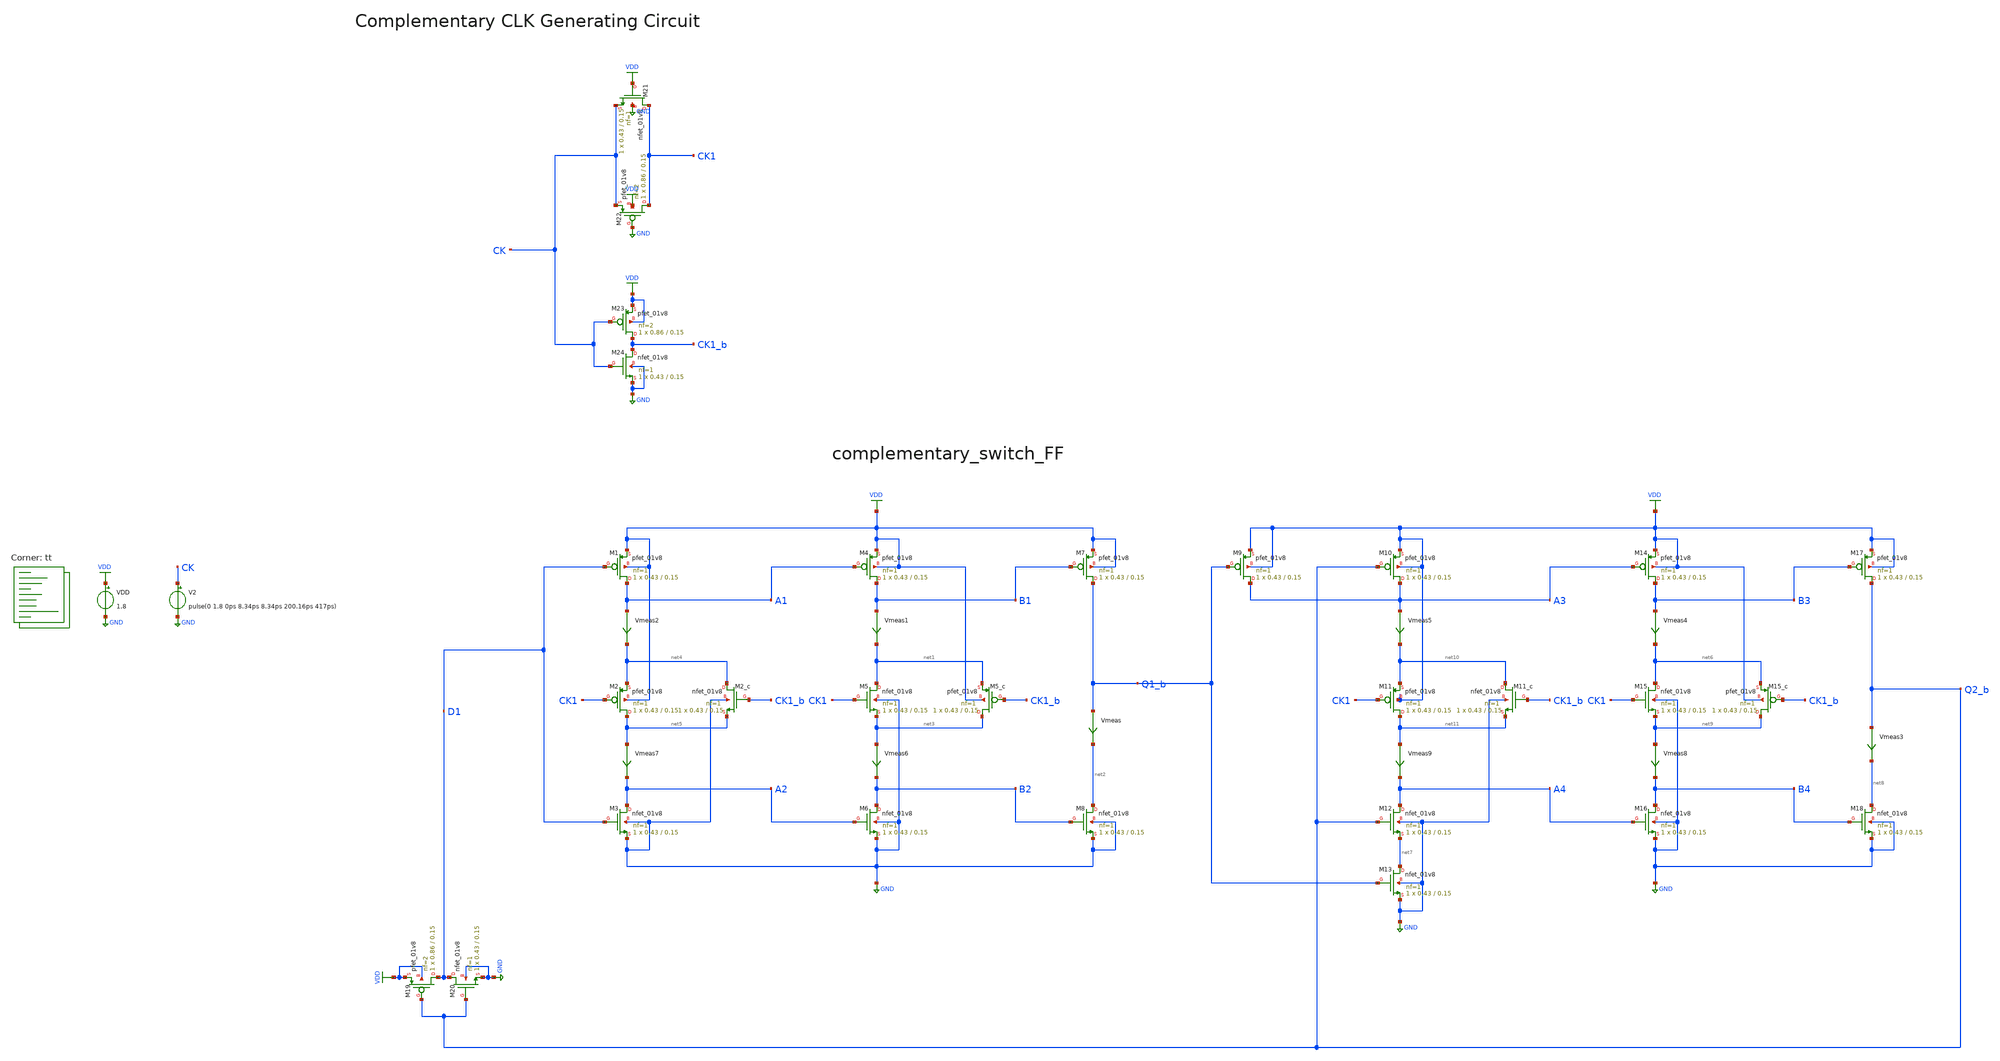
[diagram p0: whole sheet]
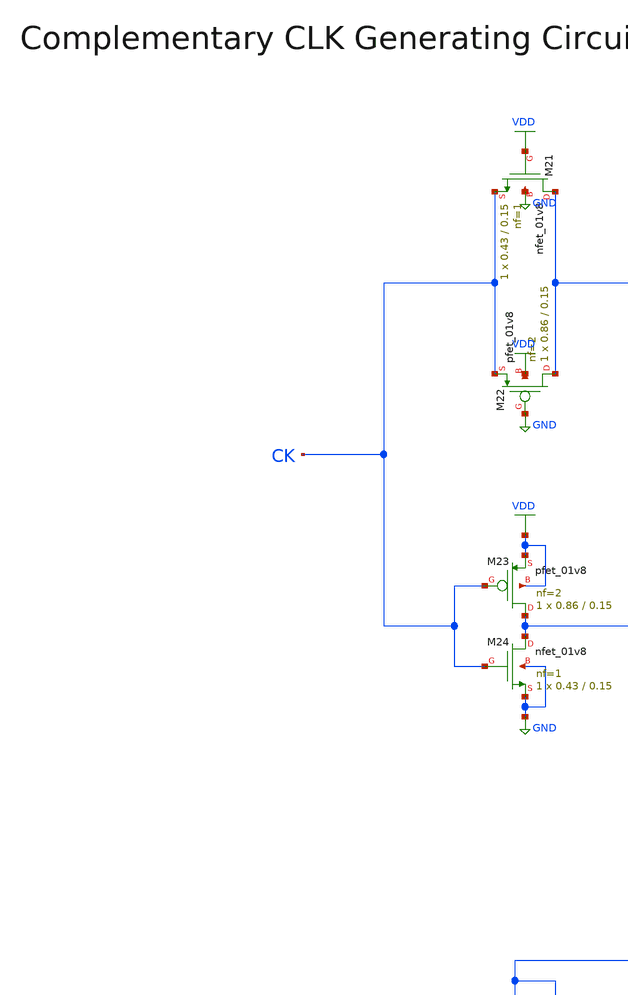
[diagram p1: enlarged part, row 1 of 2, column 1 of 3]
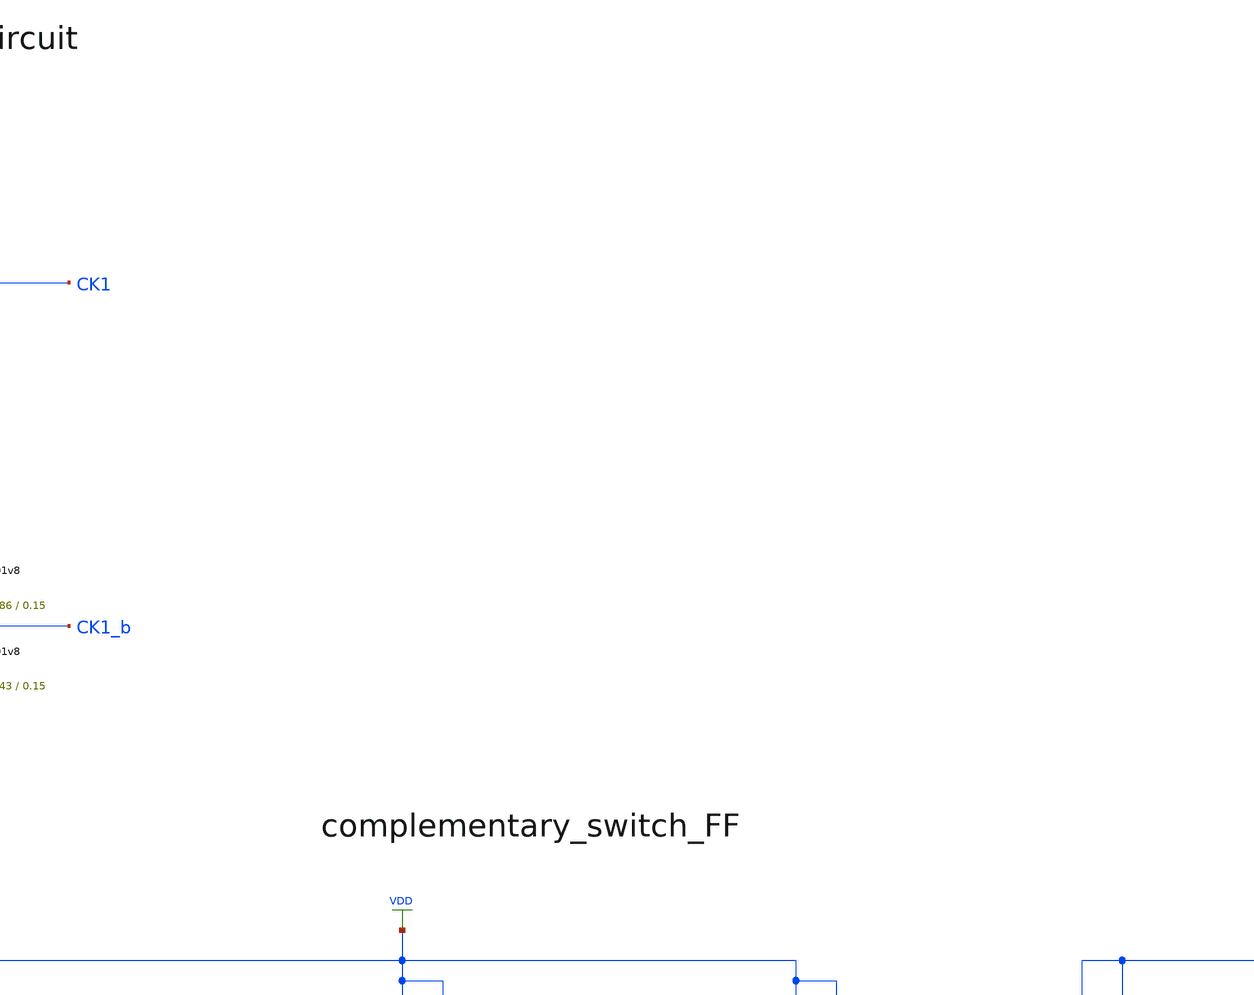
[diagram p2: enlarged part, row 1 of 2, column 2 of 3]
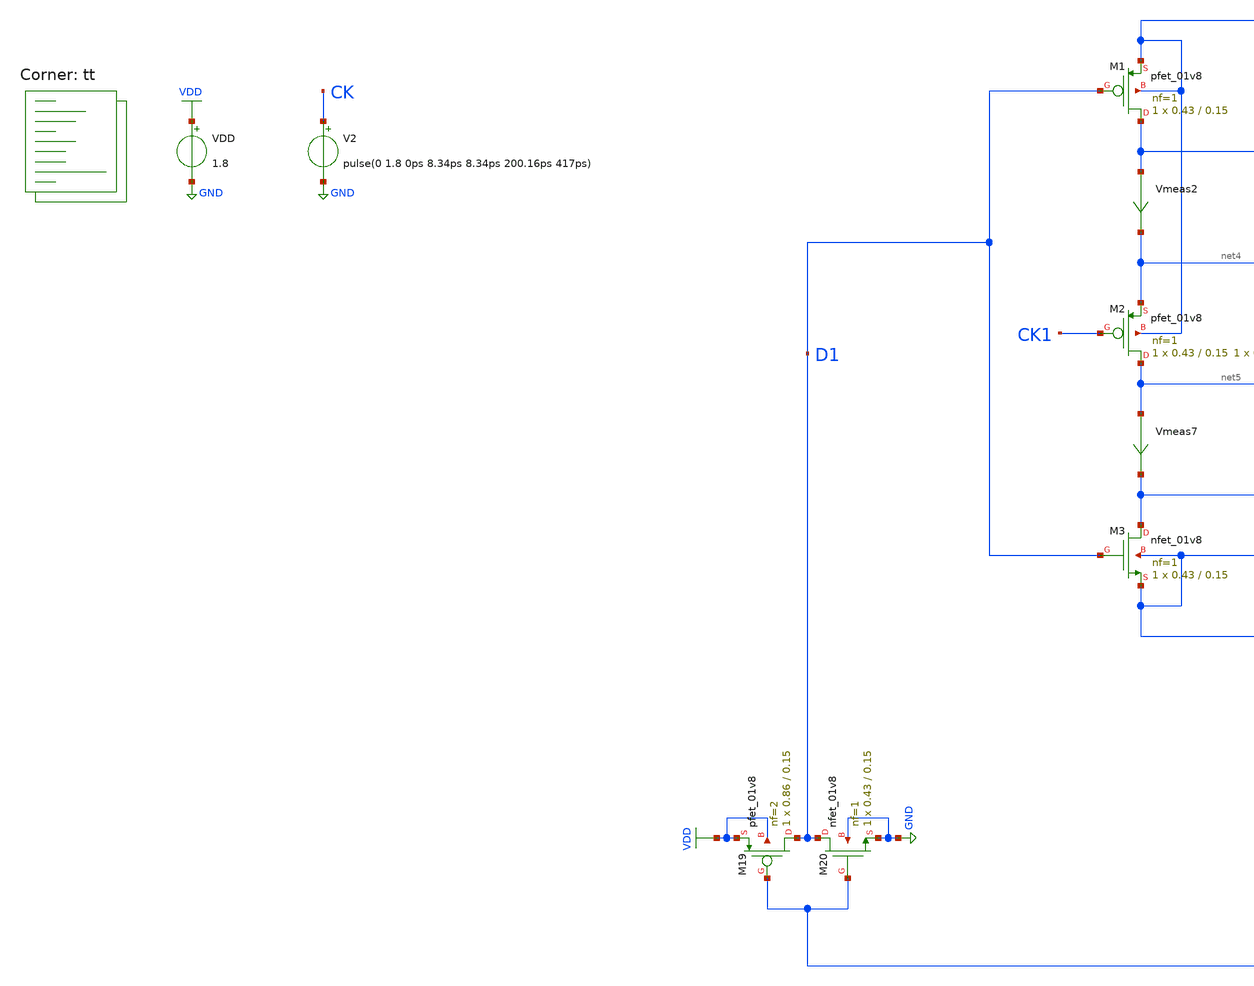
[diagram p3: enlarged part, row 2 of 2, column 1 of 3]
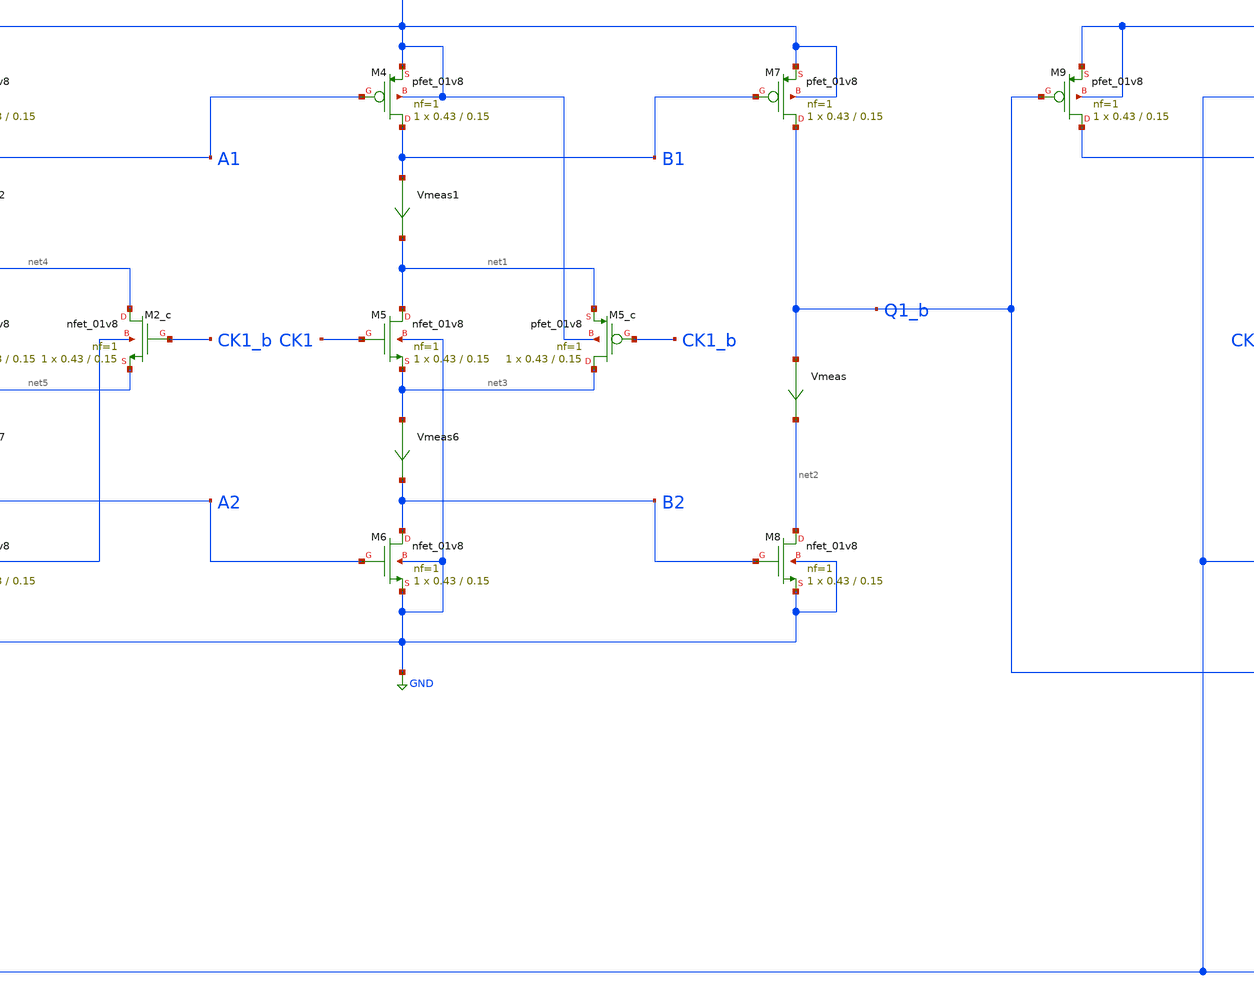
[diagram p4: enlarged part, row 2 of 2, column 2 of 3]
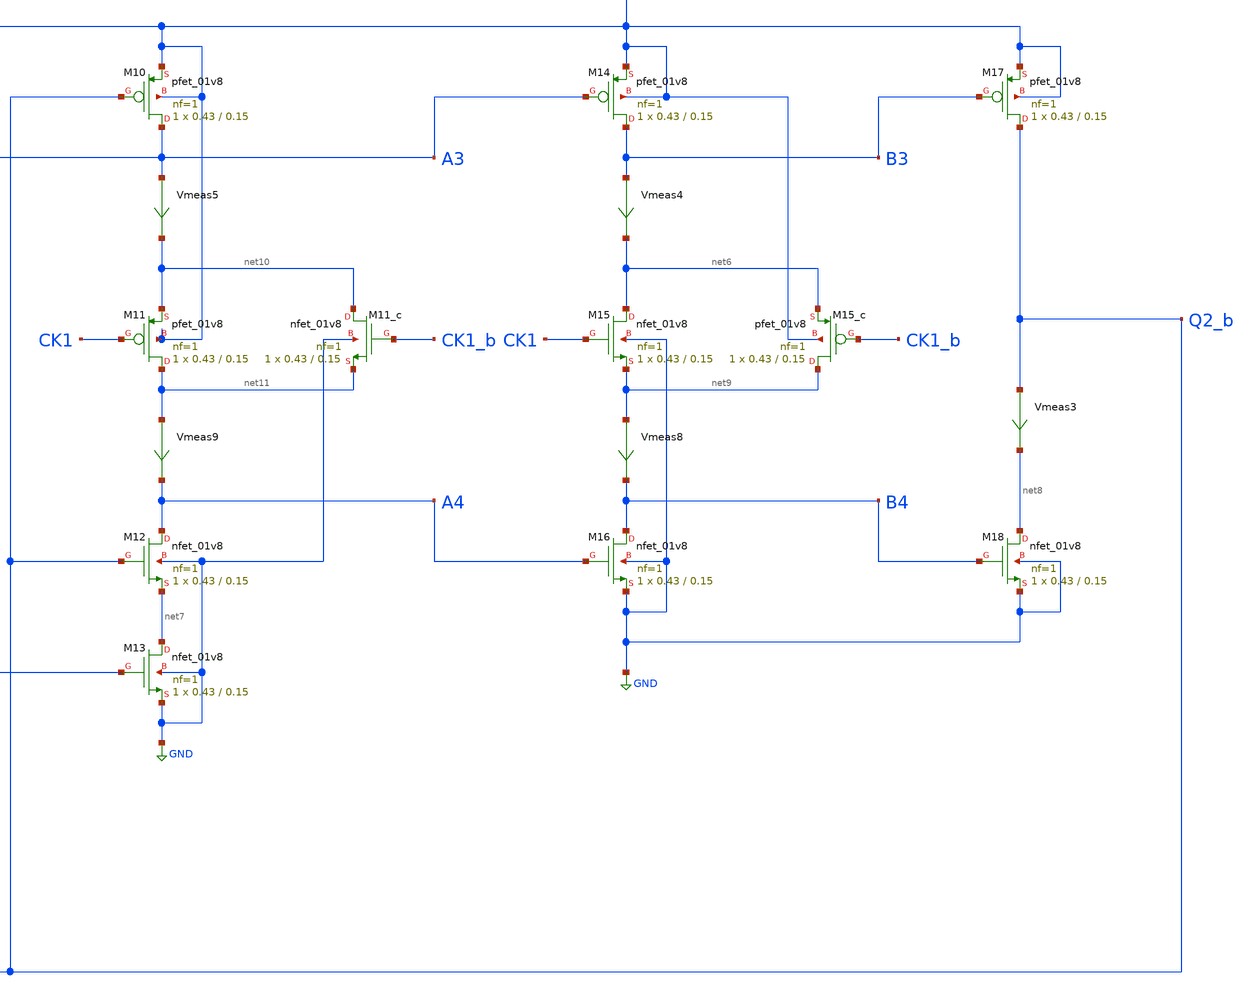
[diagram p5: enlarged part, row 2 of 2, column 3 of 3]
** sch_path: projects/pll/divider/xschem_ngspice/tb_TSPC_FF_comp_sw_divide3_3.sch
**.subckt tb_TSPC_FF_comp_sw_divide3_3
VDD VDD GND 1.8
XM7 Q1_b B1 VDD VDD sky130_fd_pr__pfet_01v8 L=0.15 W=0.43 nf=1 ad='int((nf+1)/2) * W/nf * 0.29' as='int((nf+2)/2) * W/nf * 0.29'
+ pd='2*int((nf+1)/2) * (W/nf + 0.29)' ps='2*int((nf+2)/2) * (W/nf + 0.29)' nrd='0.29 / W' nrs='0.29 / W'
+ sa=0 sb=0 sd=0 mult=1 m=1
XM5 net1 CK1 net3 GND sky130_fd_pr__nfet_01v8 L=0.15 W=0.43 nf=1 ad='int((nf+1)/2) * W/nf * 0.29' as='int((nf+2)/2) * W/nf * 0.29'
+ pd='2*int((nf+1)/2) * (W/nf + 0.29)' ps='2*int((nf+2)/2) * (W/nf + 0.29)' nrd='0.29 / W' nrs='0.29 / W'
+ sa=0 sb=0 sd=0 mult=1 m=1
Vmeas Q1_b net2 0
.save i(vmeas)
XM8 net2 B2 GND GND sky130_fd_pr__nfet_01v8 L=0.15 W=0.43 nf=1 ad='int((nf+1)/2) * W/nf * 0.29' as='int((nf+2)/2) * W/nf * 0.29'
+ pd='2*int((nf+1)/2) * (W/nf + 0.29)' ps='2*int((nf+2)/2) * (W/nf + 0.29)' nrd='0.29 / W' nrs='0.29 / W'
+ sa=0 sb=0 sd=0 mult=1 m=1
XM4 B1 A1 VDD VDD sky130_fd_pr__pfet_01v8 L=0.15 W=0.43 nf=1 ad='int((nf+1)/2) * W/nf * 0.29' as='int((nf+2)/2) * W/nf * 0.29'
+ pd='2*int((nf+1)/2) * (W/nf + 0.29)' ps='2*int((nf+2)/2) * (W/nf + 0.29)' nrd='0.29 / W' nrs='0.29 / W'
+ sa=0 sb=0 sd=0 mult=1 m=1
XM6 B2 A2 GND GND sky130_fd_pr__nfet_01v8 L=0.15 W=0.43 nf=1 ad='int((nf+1)/2) * W/nf * 0.29' as='int((nf+2)/2) * W/nf * 0.29'
+ pd='2*int((nf+1)/2) * (W/nf + 0.29)' ps='2*int((nf+2)/2) * (W/nf + 0.29)' nrd='0.29 / W' nrs='0.29 / W'
+ sa=0 sb=0 sd=0 mult=1 m=1
Vmeas1 B1 net1 0
.save i(vmeas1)
XM1 A1 D1 VDD VDD sky130_fd_pr__pfet_01v8 L=0.15 W=0.43 nf=1 ad='int((nf+1)/2) * W/nf * 0.29' as='int((nf+2)/2) * W/nf * 0.29'
+ pd='2*int((nf+1)/2) * (W/nf + 0.29)' ps='2*int((nf+2)/2) * (W/nf + 0.29)' nrd='0.29 / W' nrs='0.29 / W'
+ sa=0 sb=0 sd=0 mult=1 m=1
XM3 A2 D1 GND GND sky130_fd_pr__nfet_01v8 L=0.15 W=0.43 nf=1 ad='int((nf+1)/2) * W/nf * 0.29' as='int((nf+2)/2) * W/nf * 0.29'
+ pd='2*int((nf+1)/2) * (W/nf + 0.29)' ps='2*int((nf+2)/2) * (W/nf + 0.29)' nrd='0.29 / W' nrs='0.29 / W'
+ sa=0 sb=0 sd=0 mult=1 m=1
Vmeas2 A1 net4 0
.save i(vmeas2)
XM2 net5 CK1 net4 VDD sky130_fd_pr__pfet_01v8 L=0.15 W=0.43 nf=1 ad='int((nf+1)/2) * W/nf * 0.29' as='int((nf+2)/2) * W/nf * 0.29'
+ pd='2*int((nf+1)/2) * (W/nf + 0.29)' ps='2*int((nf+2)/2) * (W/nf + 0.29)' nrd='0.29 / W' nrs='0.29 / W'
+ sa=0 sb=0 sd=0 mult=1 m=1
XM5_c net3 CK1_b net1 VDD sky130_fd_pr__pfet_01v8 L=0.15 W=0.43 nf=1 ad='int((nf+1)/2) * W/nf * 0.29'
+ as='int((nf+2)/2) * W/nf * 0.29' pd='2*int((nf+1)/2) * (W/nf + 0.29)' ps='2*int((nf+2)/2) * (W/nf + 0.29)'
+ nrd='0.29 / W' nrs='0.29 / W' sa=0 sb=0 sd=0 mult=1 m=1
XM2_c net4 CK1_b net5 GND sky130_fd_pr__nfet_01v8 L=0.15 W=0.43 nf=1 ad='int((nf+1)/2) * W/nf * 0.29'
+ as='int((nf+2)/2) * W/nf * 0.29' pd='2*int((nf+1)/2) * (W/nf + 0.29)' ps='2*int((nf+2)/2) * (W/nf + 0.29)'
+ nrd='0.29 / W' nrs='0.29 / W' sa=0 sb=0 sd=0 mult=1 m=1
XM22 CK1 GND CK VDD sky130_fd_pr__pfet_01v8 L=0.15 W=0.86 nf=2 ad='int((nf+1)/2) * W/nf * 0.29' as='int((nf+2)/2) * W/nf * 0.29'
+ pd='2*int((nf+1)/2) * (W/nf + 0.29)' ps='2*int((nf+2)/2) * (W/nf + 0.29)' nrd='0.29 / W' nrs='0.29 / W'
+ sa=0 sb=0 sd=0 mult=1 m=1
XM21 CK1 VDD CK GND sky130_fd_pr__nfet_01v8 L=0.15 W=0.43 nf=1 ad='int((nf+1)/2) * W/nf * 0.29' as='int((nf+2)/2) * W/nf * 0.29'
+ pd='2*int((nf+1)/2) * (W/nf + 0.29)' ps='2*int((nf+2)/2) * (W/nf + 0.29)' nrd='0.29 / W' nrs='0.29 / W'
+ sa=0 sb=0 sd=0 mult=1 m=1
XM23 CK1_b CK VDD VDD sky130_fd_pr__pfet_01v8 L=0.15 W=0.86 nf=2 ad='int((nf+1)/2) * W/nf * 0.29' as='int((nf+2)/2) * W/nf * 0.29'
+ pd='2*int((nf+1)/2) * (W/nf + 0.29)' ps='2*int((nf+2)/2) * (W/nf + 0.29)' nrd='0.29 / W' nrs='0.29 / W'
+ sa=0 sb=0 sd=0 mult=1 m=1
XM24 CK1_b CK GND GND sky130_fd_pr__nfet_01v8 L=0.15 W=0.43 nf=1 ad='int((nf+1)/2) * W/nf * 0.29' as='int((nf+2)/2) * W/nf * 0.29'
+ pd='2*int((nf+1)/2) * (W/nf + 0.29)' ps='2*int((nf+2)/2) * (W/nf + 0.29)' nrd='0.29 / W' nrs='0.29 / W'
+ sa=0 sb=0 sd=0 mult=1 m=1
XM17 Q2_b B3 VDD VDD sky130_fd_pr__pfet_01v8 L=0.15 W=0.43 nf=1 ad='int((nf+1)/2) * W/nf * 0.29' as='int((nf+2)/2) * W/nf * 0.29'
+ pd='2*int((nf+1)/2) * (W/nf + 0.29)' ps='2*int((nf+2)/2) * (W/nf + 0.29)' nrd='0.29 / W' nrs='0.29 / W'
+ sa=0 sb=0 sd=0 mult=1 m=1
XM15 net6 CK1 net9 GND sky130_fd_pr__nfet_01v8 L=0.15 W=0.43 nf=1 ad='int((nf+1)/2) * W/nf * 0.29' as='int((nf+2)/2) * W/nf * 0.29'
+ pd='2*int((nf+1)/2) * (W/nf + 0.29)' ps='2*int((nf+2)/2) * (W/nf + 0.29)' nrd='0.29 / W' nrs='0.29 / W'
+ sa=0 sb=0 sd=0 mult=1 m=1
Vmeas3 Q2_b net8 0
.save i(vmeas3)
XM18 net8 B4 GND GND sky130_fd_pr__nfet_01v8 L=0.15 W=0.43 nf=1 ad='int((nf+1)/2) * W/nf * 0.29' as='int((nf+2)/2) * W/nf * 0.29'
+ pd='2*int((nf+1)/2) * (W/nf + 0.29)' ps='2*int((nf+2)/2) * (W/nf + 0.29)' nrd='0.29 / W' nrs='0.29 / W'
+ sa=0 sb=0 sd=0 mult=1 m=1
XM14 B3 A3 VDD VDD sky130_fd_pr__pfet_01v8 L=0.15 W=0.43 nf=1 ad='int((nf+1)/2) * W/nf * 0.29' as='int((nf+2)/2) * W/nf * 0.29'
+ pd='2*int((nf+1)/2) * (W/nf + 0.29)' ps='2*int((nf+2)/2) * (W/nf + 0.29)' nrd='0.29 / W' nrs='0.29 / W'
+ sa=0 sb=0 sd=0 mult=1 m=1
XM16 B4 A4 GND GND sky130_fd_pr__nfet_01v8 L=0.15 W=0.43 nf=1 ad='int((nf+1)/2) * W/nf * 0.29' as='int((nf+2)/2) * W/nf * 0.29'
+ pd='2*int((nf+1)/2) * (W/nf + 0.29)' ps='2*int((nf+2)/2) * (W/nf + 0.29)' nrd='0.29 / W' nrs='0.29 / W'
+ sa=0 sb=0 sd=0 mult=1 m=1
Vmeas4 B3 net6 0
.save i(vmeas4)
XM10 A3 Q2_b VDD VDD sky130_fd_pr__pfet_01v8 L=0.15 W=0.43 nf=1 ad='int((nf+1)/2) * W/nf * 0.29' as='int((nf+2)/2) * W/nf * 0.29'
+ pd='2*int((nf+1)/2) * (W/nf + 0.29)' ps='2*int((nf+2)/2) * (W/nf + 0.29)' nrd='0.29 / W' nrs='0.29 / W'
+ sa=0 sb=0 sd=0 mult=1 m=1
XM12 A4 Q2_b net7 GND sky130_fd_pr__nfet_01v8 L=0.15 W=0.43 nf=1 ad='int((nf+1)/2) * W/nf * 0.29' as='int((nf+2)/2) * W/nf * 0.29'
+ pd='2*int((nf+1)/2) * (W/nf + 0.29)' ps='2*int((nf+2)/2) * (W/nf + 0.29)' nrd='0.29 / W' nrs='0.29 / W'
+ sa=0 sb=0 sd=0 mult=1 m=1
Vmeas5 A3 net10 0
.save i(vmeas5)
XM11 net11 CK1 net10 VDD sky130_fd_pr__pfet_01v8 L=0.15 W=0.43 nf=1 ad='int((nf+1)/2) * W/nf * 0.29'
+ as='int((nf+2)/2) * W/nf * 0.29' pd='2*int((nf+1)/2) * (W/nf + 0.29)' ps='2*int((nf+2)/2) * (W/nf + 0.29)'
+ nrd='0.29 / W' nrs='0.29 / W' sa=0 sb=0 sd=0 mult=1 m=1
XM15_c net9 CK1_b net6 VDD sky130_fd_pr__pfet_01v8 L=0.15 W=0.43 nf=1 ad='int((nf+1)/2) * W/nf * 0.29'
+ as='int((nf+2)/2) * W/nf * 0.29' pd='2*int((nf+1)/2) * (W/nf + 0.29)' ps='2*int((nf+2)/2) * (W/nf + 0.29)'
+ nrd='0.29 / W' nrs='0.29 / W' sa=0 sb=0 sd=0 mult=1 m=1
XM11_c net10 CK1_b net11 GND sky130_fd_pr__nfet_01v8 L=0.15 W=0.43 nf=1 ad='int((nf+1)/2) * W/nf * 0.29'
+ as='int((nf+2)/2) * W/nf * 0.29' pd='2*int((nf+1)/2) * (W/nf + 0.29)' ps='2*int((nf+2)/2) * (W/nf + 0.29)'
+ nrd='0.29 / W' nrs='0.29 / W' sa=0 sb=0 sd=0 mult=1 m=1
Vmeas6 net3 B2 0
.save i(vmeas6)
Vmeas7 net5 A2 0
.save i(vmeas7)
Vmeas8 net9 B4 0
.save i(vmeas8)
Vmeas9 net11 A4 0
.save i(vmeas9)
V2 CK GND pulse(0 1.8 0ps 8.34ps 8.34ps 200.16ps 417ps)
XM19 D1 Q2_b VDD VDD sky130_fd_pr__pfet_01v8 L=0.15 W=0.86 nf=2 ad='int((nf+1)/2) * W/nf * 0.29' as='int((nf+2)/2) * W/nf * 0.29'
+ pd='2*int((nf+1)/2) * (W/nf + 0.29)' ps='2*int((nf+2)/2) * (W/nf + 0.29)' nrd='0.29 / W' nrs='0.29 / W'
+ sa=0 sb=0 sd=0 mult=1 m=1
XM20 D1 Q2_b GND GND sky130_fd_pr__nfet_01v8 L=0.15 W=0.43 nf=1 ad='int((nf+1)/2) * W/nf * 0.29' as='int((nf+2)/2) * W/nf * 0.29'
+ pd='2*int((nf+1)/2) * (W/nf + 0.29)' ps='2*int((nf+2)/2) * (W/nf + 0.29)' nrd='0.29 / W' nrs='0.29 / W'
+ sa=0 sb=0 sd=0 mult=1 m=1
XM9 A3 Q1_b VDD VDD sky130_fd_pr__pfet_01v8 L=0.15 W=0.43 nf=1 ad='int((nf+1)/2) * W/nf * 0.29' as='int((nf+2)/2) * W/nf * 0.29'
+ pd='2*int((nf+1)/2) * (W/nf + 0.29)' ps='2*int((nf+2)/2) * (W/nf + 0.29)' nrd='0.29 / W' nrs='0.29 / W'
+ sa=0 sb=0 sd=0 mult=1 m=1
XM13 net7 Q1_b GND GND sky130_fd_pr__nfet_01v8 L=0.15 W=0.43 nf=1 ad='int((nf+1)/2) * W/nf * 0.29' as='int((nf+2)/2) * W/nf * 0.29'
+ pd='2*int((nf+1)/2) * (W/nf + 0.29)' ps='2*int((nf+2)/2) * (W/nf + 0.29)' nrd='0.29 / W' nrs='0.29 / W'
+ sa=0 sb=0 sd=0 mult=1 m=1
**** begin user architecture code



.option method=gear
.option wnflag=1

.control

  save all
  tran 5p 20n
  remzerovec
  write tb_TSPC_FF_comp_sw_divide3_3.raw
  set appendwrite

.endc



.lib $::SKYWATER_MODELS/sky130.lib.spice tt
**** end user architecture code
**.ends
.GLOBAL GND
.GLOBAL VDD
.end
